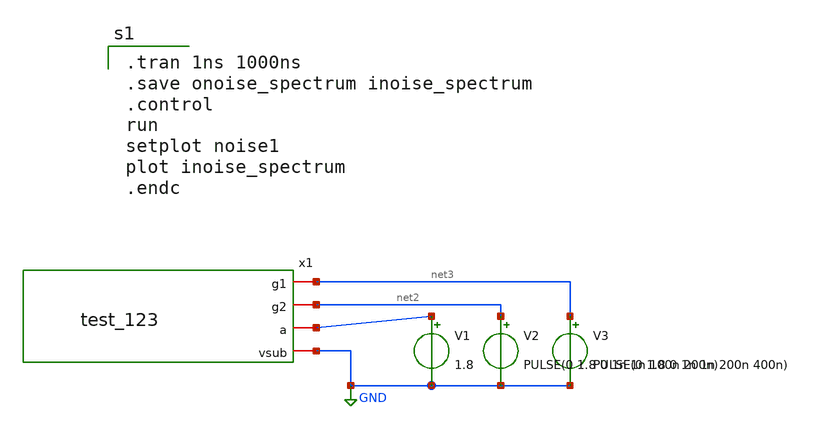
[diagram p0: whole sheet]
** sch_path: xschem/test_234.sch
**.subckt test_234
x1 net3 net2 net1 GND test_123
V1 net1 GND 1.8
V2 net2 GND PULSE(0 1.8 0 1n 1n 100n 200n)
V3 net3 GND PULSE(0 1.8 0 1n 1n 200n 400n)
**** begin user architecture code
.lib $::SKYWATER_MODELS/sky130.lib.spice tt
.include $::PDKPATH/libs.ref/sky130_fd_sc_hs/spice/sky130_fd_sc_hs.spice


.tran 1ns 1000ns
.save onoise_spectrum inoise_spectrum
.control
run
setplot noise1
plot inoise_spectrum
.endc


**** end user architecture code
**.ends

* expanding   symbol:  test_123.sym # of pins=4
** sym_path: xschem/test_123.sym
** sch_path: xschem/test_123.sch
.subckt test_123 g1 g2 a vsub
*.iopin g1
*.iopin g2
*.iopin a
*.iopin vsub
**** begin user architecture code

.subckt test_123 G1 G2 A VSUBS

    X0 VSUBS G2 A VSUBS sky130_fd_pr__nfet_01v8 ad=0p pd=0u as=0p ps=0u w=1e+07u l=150000u
    X1 A G1 VSUBS VSUBS sky130_fd_pr__nfet_01v8 ad=0p pd=0u as=0p ps=0u w=1e+07u l=150000u
    C0 G1 G2 0.01fF
    C1 A G2 0.01fF
    C2 G1 A 0.02fF
    C3 A VSUBS 3.23fF $ **FLOATING
    C4 G1 VSUBS 0.26fF $ **FLOATING
    C5 G2 VSUBS 0.27fF $ **FLOATING
.ends

XDUT g1 g2 a vsubs test_123


**** end user architecture code
.ends

.GLOBAL GND
.end
